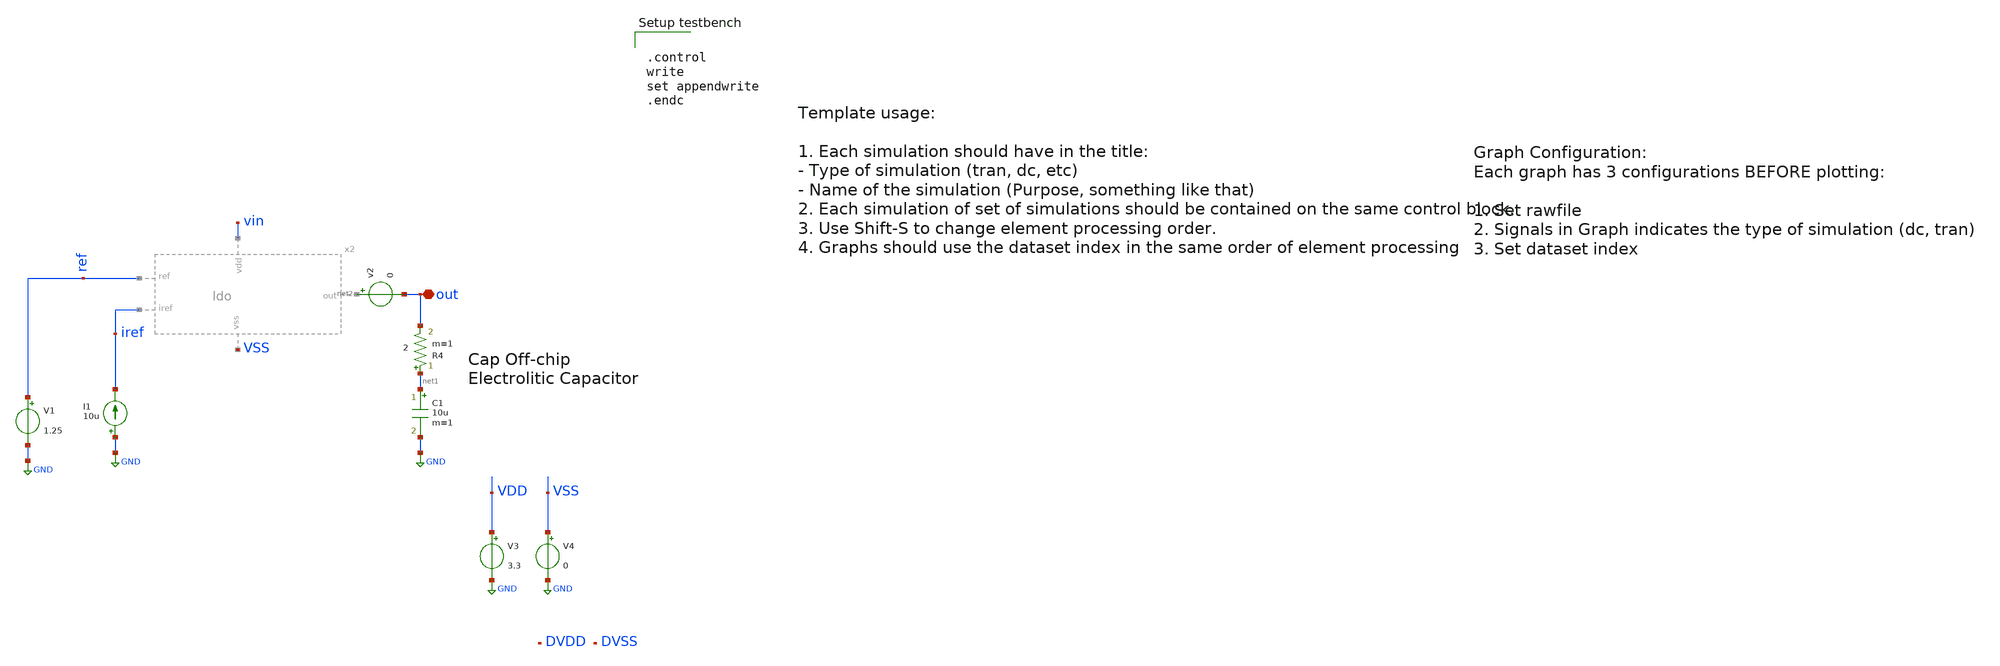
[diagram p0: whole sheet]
** sch_path: LDO/xschem/ldo/test/line_regulation.sch

.include $env(PDK_ROOT)/$env(PDK)/libs.tech/ngspice/design.ngspice
.lib $env(PDK_ROOT)/$env(PDK)/libs.tech/ngspice/sm141064.ngspice typical
.lib $env(PDK_ROOT)/$env(PDK)/libs.tech/ngspice/sm141064.ngspice res_typical
.lib $env(PDK_ROOT)/$env(PDK)/libs.tech/ngspice/sm141064.ngspice diode_typical
.lib $env(PDK_ROOT)/$env(PDK)/libs.tech/ngspice/sm141064.ngspice bjt_typical
.lib $env(PDK_ROOT)/$env(PDK)/libs.tech/ngspice/sm141064.ngspice cap_mim
.lib $env(PDK_ROOT)/$env(PDK)/libs.tech/ngspice/sm141064.ngspice moscap_typical
.lib $env(PDK_ROOT)/$env(PDK)/libs.tech/ngspice/sm141064.ngspice mimcap_typical

.include $env(PDK_ROOT)/$env(PDK)/libs.ref/gf180mcu_fd_io/spice/gf180mcu_fd_io.spice


.control
write
set appendwrite
.endc


**.subckt line_regulation out
*.iopin out
I1 GND iref 10u
V1 ref GND 1.25
v2 net2 out 0
C1 net1 GND 10u m=1
R4 net1 out 2 m=1
V3 VDD GND 3.3
V4 VSS GND 0
**** begin user architecture code


.param R=33
R10 out 0 {R}
IL out 0 PWL(0 0.1m 10u 0.1m 20u 10m 30u 10m)

.param iref = 10u
.param vdd  = 5
.param vss  = 0.0
.param vcm  = 1.25
.param vac  = 60m
.param w857 = 5u
.param l857 = 1u
.param m857 = 1
.param wpar = 10u
.param lpar = 1u
.param mpar = 1
.param w34  = 10u
.param l34  = 1u
.param m34  = 1
.param w6   = 100u
.param l6   = 1u
.param m6   = 1

.param m5   = 1
.param m7   = 5


Vs vin 0 5

.nodeset v(out)=0
.nodeset v(x2.feedback)=0

*supply_sweep
.control
save vin out
alter IL 0
dc Vs 6 0 -0.001
plot v(vin) v(out)
meas DC vldo_sup_4_6 FIND v(out) AT=4.6
meas DC vldo_nom FIND v(out) AT=5
meas DC vldo_sup_5_4 FIND v(out) AT=5.4
let line_reg = abs((vldo_sup_5_4-vldo_sup_4_6)/0.8)
print line_reg
meas DC vin WHEN v(out)=3.2982
let dropout = vin-3.2982
print dropout

write
.endc




.include ../../../spice/ldo_clean.spice
.include ../../../spice/ldo_pex.spice

*Xvdd DVDD DVSS VSS gf180mcu_fd_io__dvdd
*Xvss DVDD DVSS VDD gf180mcu_fd_io__dvss

*Xiref iref DVDD DVSS VDD VSS gf180mcu_fd_io__asig_5p0
*Xref  ref  DVDD DVSS VDD VSS gf180mcu_fd_io__asig_5p0
*Xout  out  DVDD DVSS VDD VSS gf180mcu_fd_io__asig_5p0



*** writing format= xdevice vdd ref iref out vss ldo_*

*** for using this SPICE extracted netlists, you may change spice_ignore
*** value to 1 in the LDO symbol (this way you will bypass the prelayout LDO)

*** for clean layout simulation

*x2 vin ref iref out GND ldo_clean

*** for parasitic extraction simulation

x2 vin ref iref out GND ldo_pex


**** end user architecture code
**.ends
.GLOBAL GND
.end
